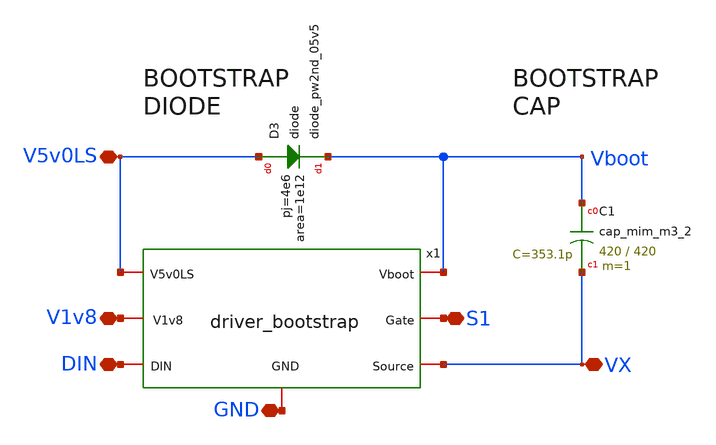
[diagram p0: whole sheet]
** sch_path: xschem/top_driver.sch
**.subckt top_driver V5v0LS V1v8 GND DIN S1 VX
*.iopin V5v0LS
*.iopin V1v8
*.iopin GND
*.iopin DIN
*.iopin S1
*.iopin VX
x1 Vboot S1 VX V5v0LS V1v8 GND DIN driver_bootstrap
XD3 V5v0LS Vboot sky130_fd_pr__diode_pw2nd_05v5 area=1e12 pj=4e6
XC1 Vboot VX sky130_fd_pr__cap_mim_m3_2 W=420 L=420 MF=1 m=1
**.ends
.end
